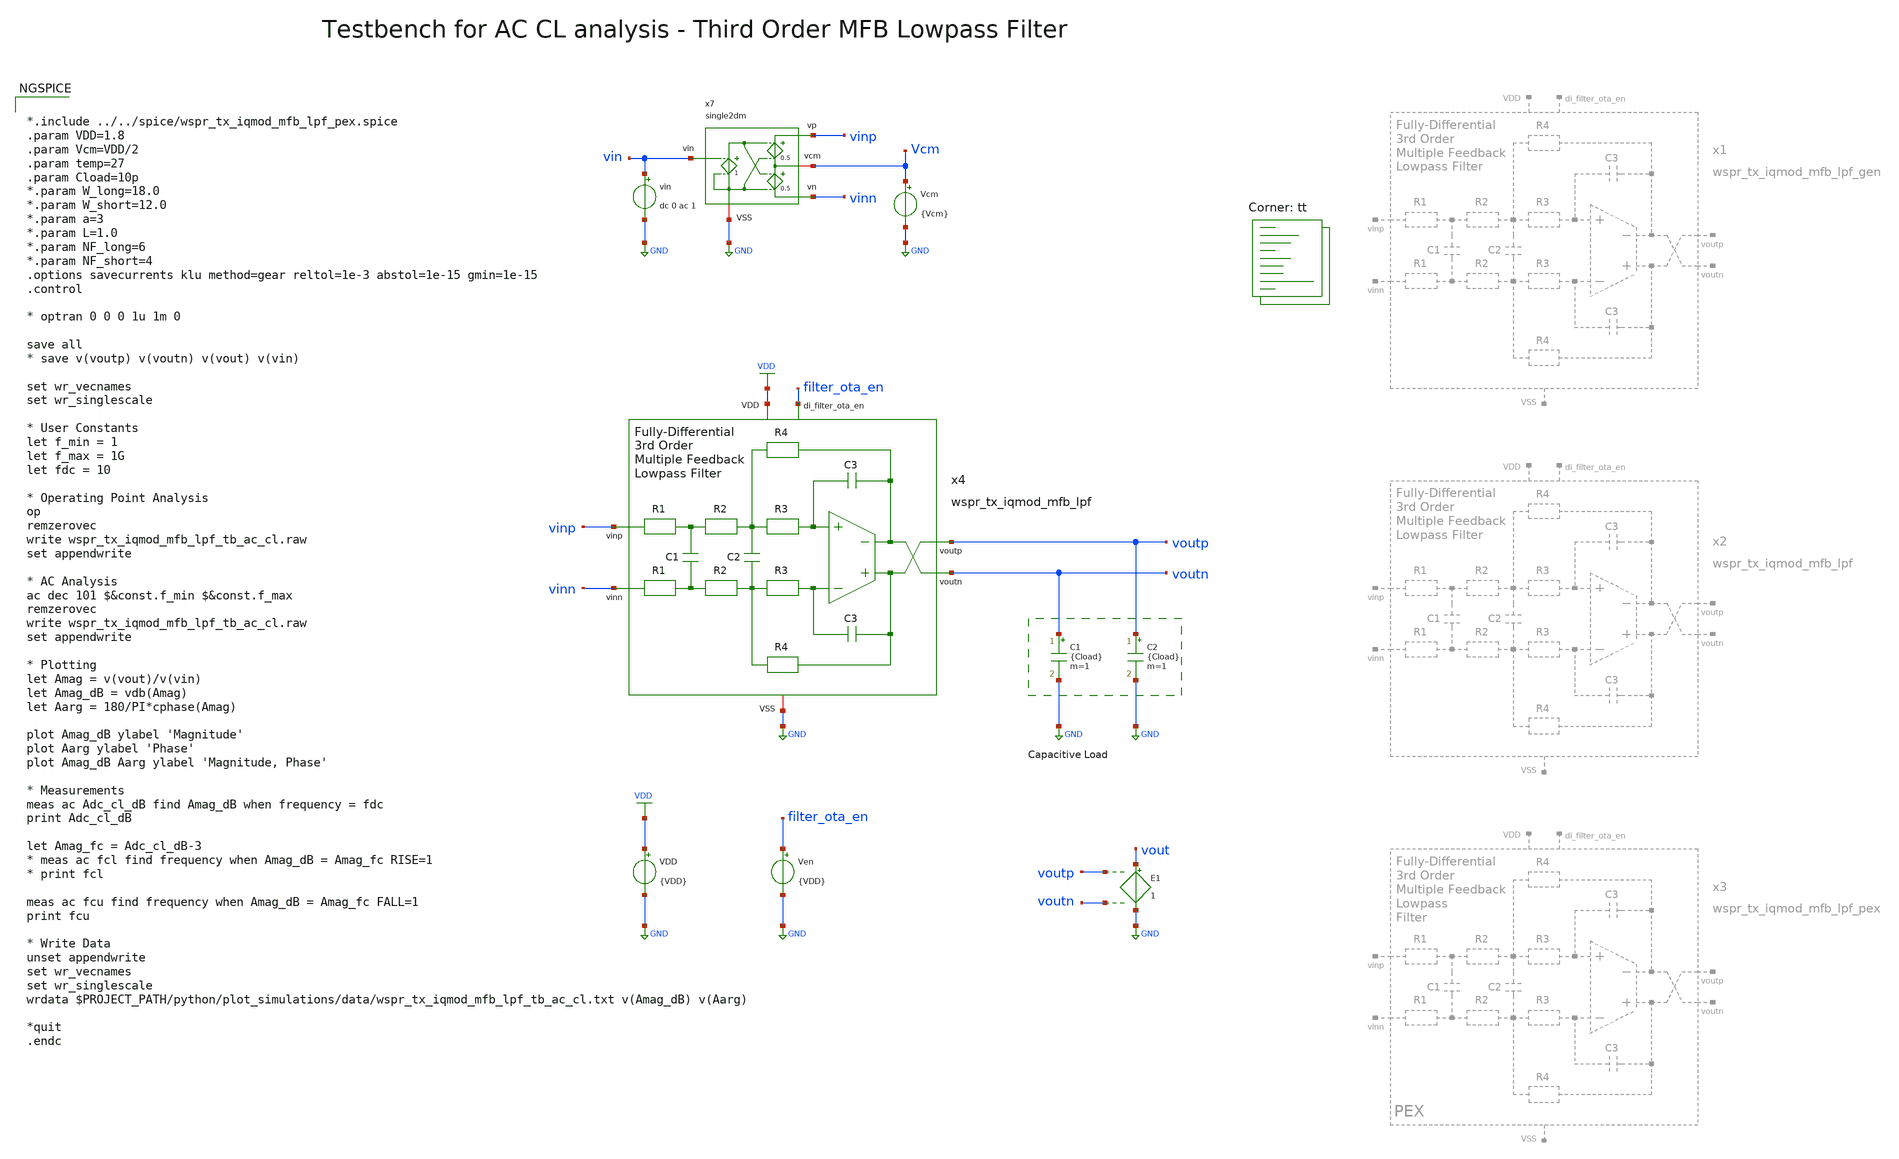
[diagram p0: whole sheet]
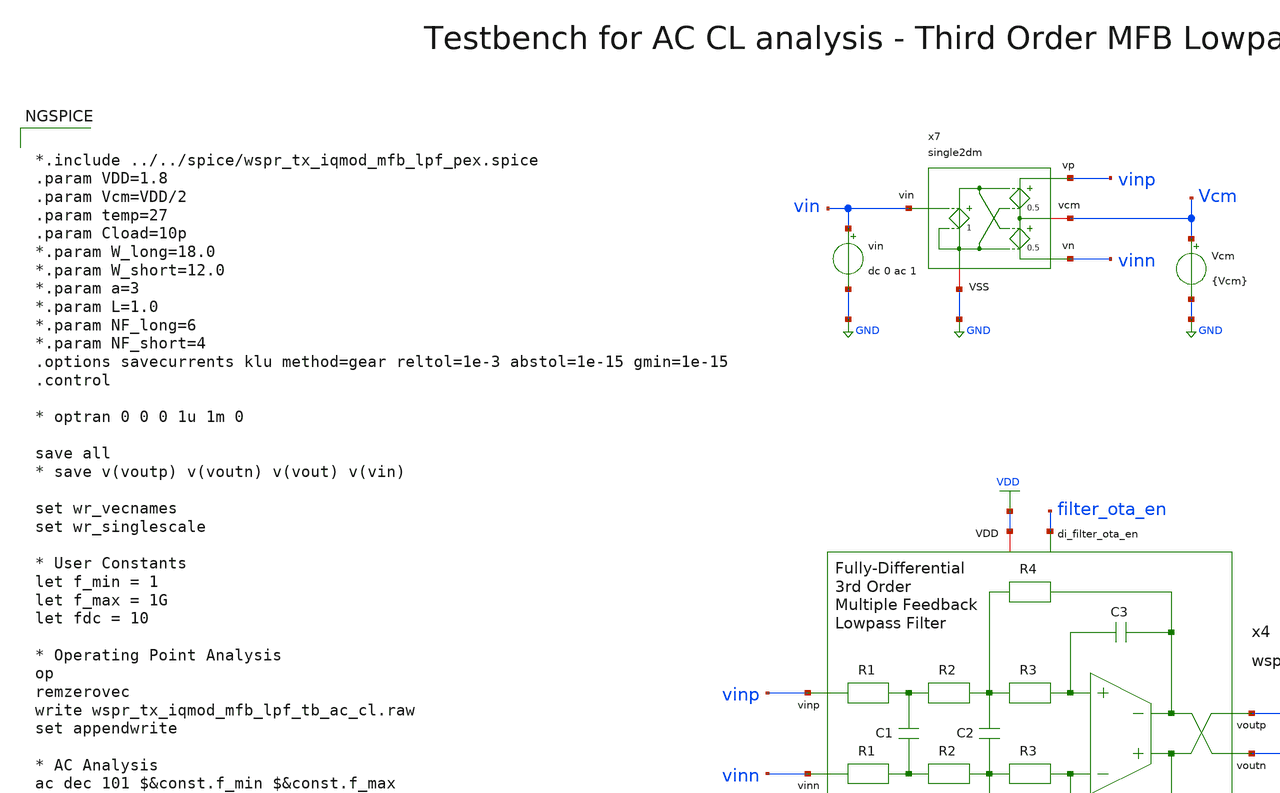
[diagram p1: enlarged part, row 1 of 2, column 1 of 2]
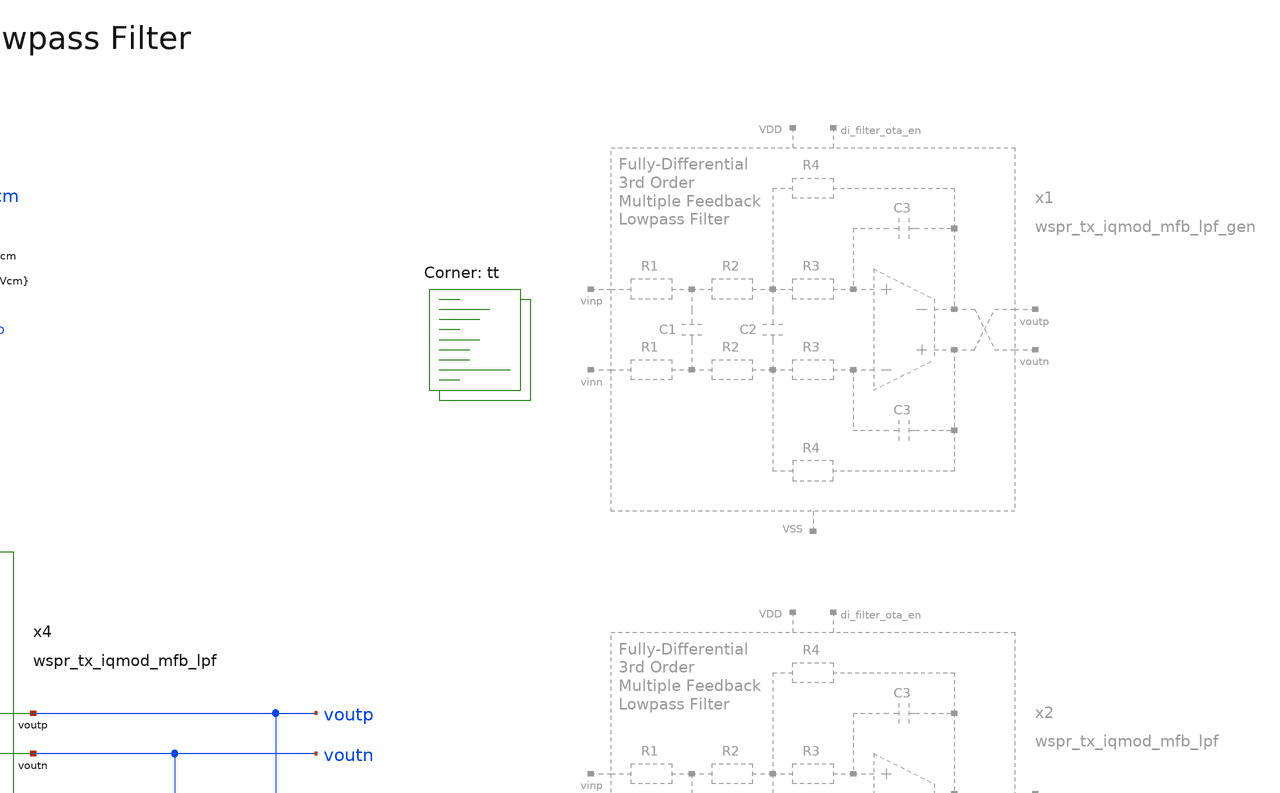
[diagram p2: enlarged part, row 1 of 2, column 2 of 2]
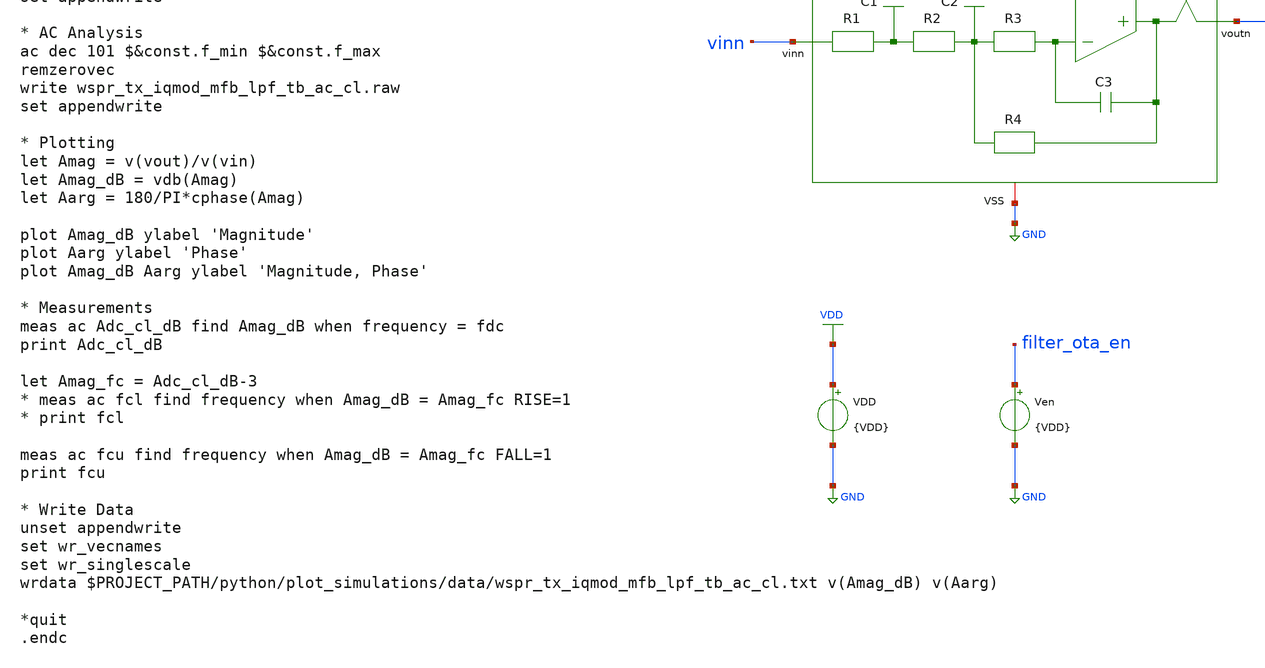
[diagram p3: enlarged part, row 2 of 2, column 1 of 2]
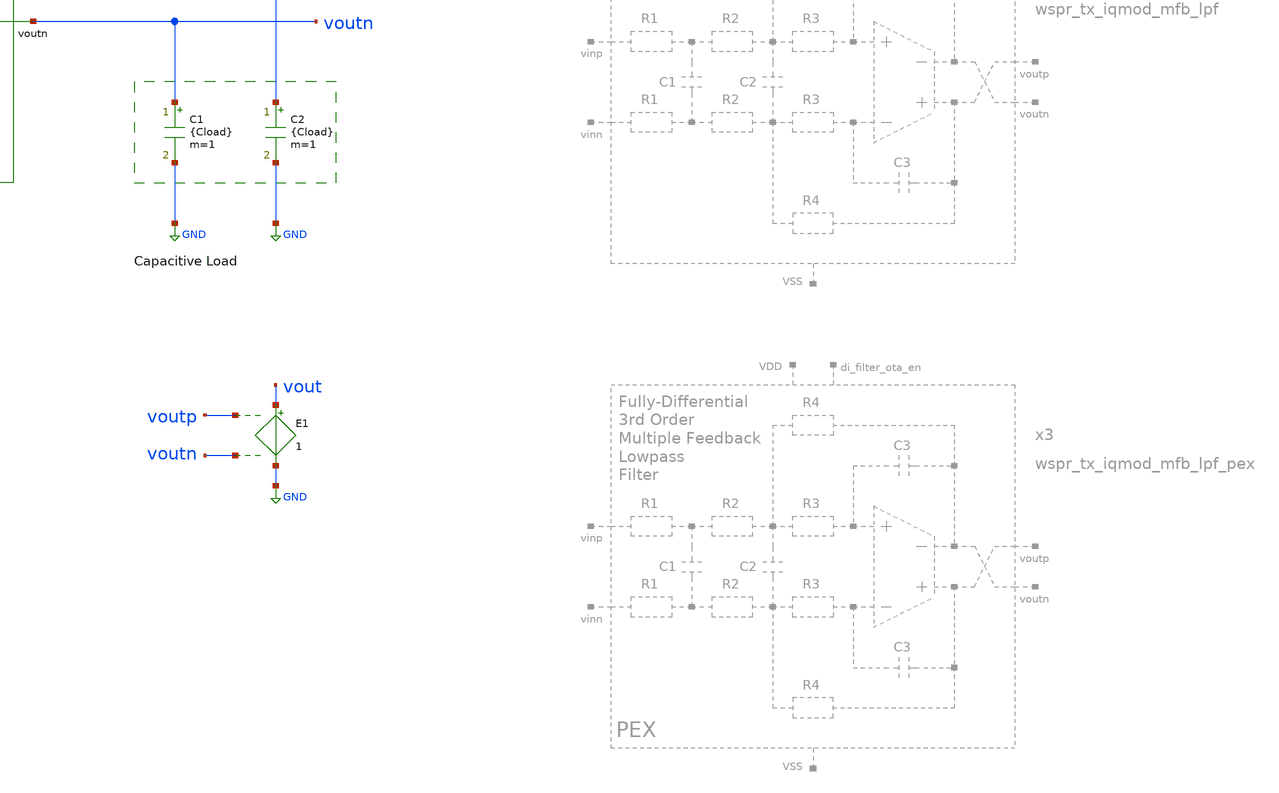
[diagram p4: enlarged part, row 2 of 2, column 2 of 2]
** sch_path: sky130/xschem/testbenches/wspr_tx_iqmod_mfb_lpf_tb_ac_cl.sch
**.subckt wspr_tx_iqmod_mfb_lpf_tb_ac_cl
VDD VDD GND {VDD}
C1 voutn GND {Cload} m=1
C2 voutp GND {Cload} m=1
Ven filter_ota_en GND {VDD}
E1 vout GND voutp voutn 1
x4 filter_ota_en voutp vinp voutn vinn VDD GND wspr_tx_iqmod_mfb_lpf
Vcm Vcm GND {Vcm}
vin vin GND dc 0 ac 1
x7 vinp vin Vcm GND vinn single2dm
**** begin user architecture code


*.include ../../spice/wspr_tx_iqmod_mfb_lpf_pex.spice
.param VDD=1.8
.param Vcm=VDD/2
.param temp=27
.param Cload=10p
*.param W_long=18.0
*.param W_short=12.0
*.param a=3
*.param L=1.0
*.param NF_long=6
*.param NF_short=4
.options savecurrents klu method=gear reltol=1e-3 abstol=1e-15 gmin=1e-15
.control

* optran 0 0 0 1u 1m 0

save all
* save v(voutp) v(voutn) v(vout) v(vin)

set wr_vecnames
set wr_singlescale

* User Constants
let f_min = 1
let f_max = 1G
let fdc = 10

* Operating Point Analysis
op
remzerovec
write wspr_tx_iqmod_mfb_lpf_tb_ac_cl.raw
set appendwrite

* AC Analysis
ac dec 101 $&const.f_min $&const.f_max
remzerovec
write wspr_tx_iqmod_mfb_lpf_tb_ac_cl.raw
set appendwrite

* Plotting
let Amag = v(vout)/v(vin)
let Amag_dB = vdb(Amag)
let Aarg = 180/PI*cphase(Amag)

plot Amag_dB ylabel 'Magnitude'
plot Aarg ylabel 'Phase'
plot Amag_dB Aarg ylabel 'Magnitude, Phase'

* Measurements
meas ac Adc_cl_dB find Amag_dB when frequency = fdc
print Adc_cl_dB

let Amag_fc = Adc_cl_dB-3
* meas ac fcl find frequency when Amag_dB = Amag_fc RISE=1
* print fcl

meas ac fcu find frequency when Amag_dB = Amag_fc FALL=1
print fcu

* Write Data
unset appendwrite
set wr_vecnames
set wr_singlescale
wrdata $PROJECT_PATH/python/plot_simulations/data/wspr_tx_iqmod_mfb_lpf_tb_ac_cl.txt v(Amag_dB)
+ v(Aarg)

*quit
.endc


.lib $::SKYWATER_MODELS/sky130.lib.spice tt
**** end user architecture code
**.ends
.GLOBAL GND
.GLOBAL VDD
.end
